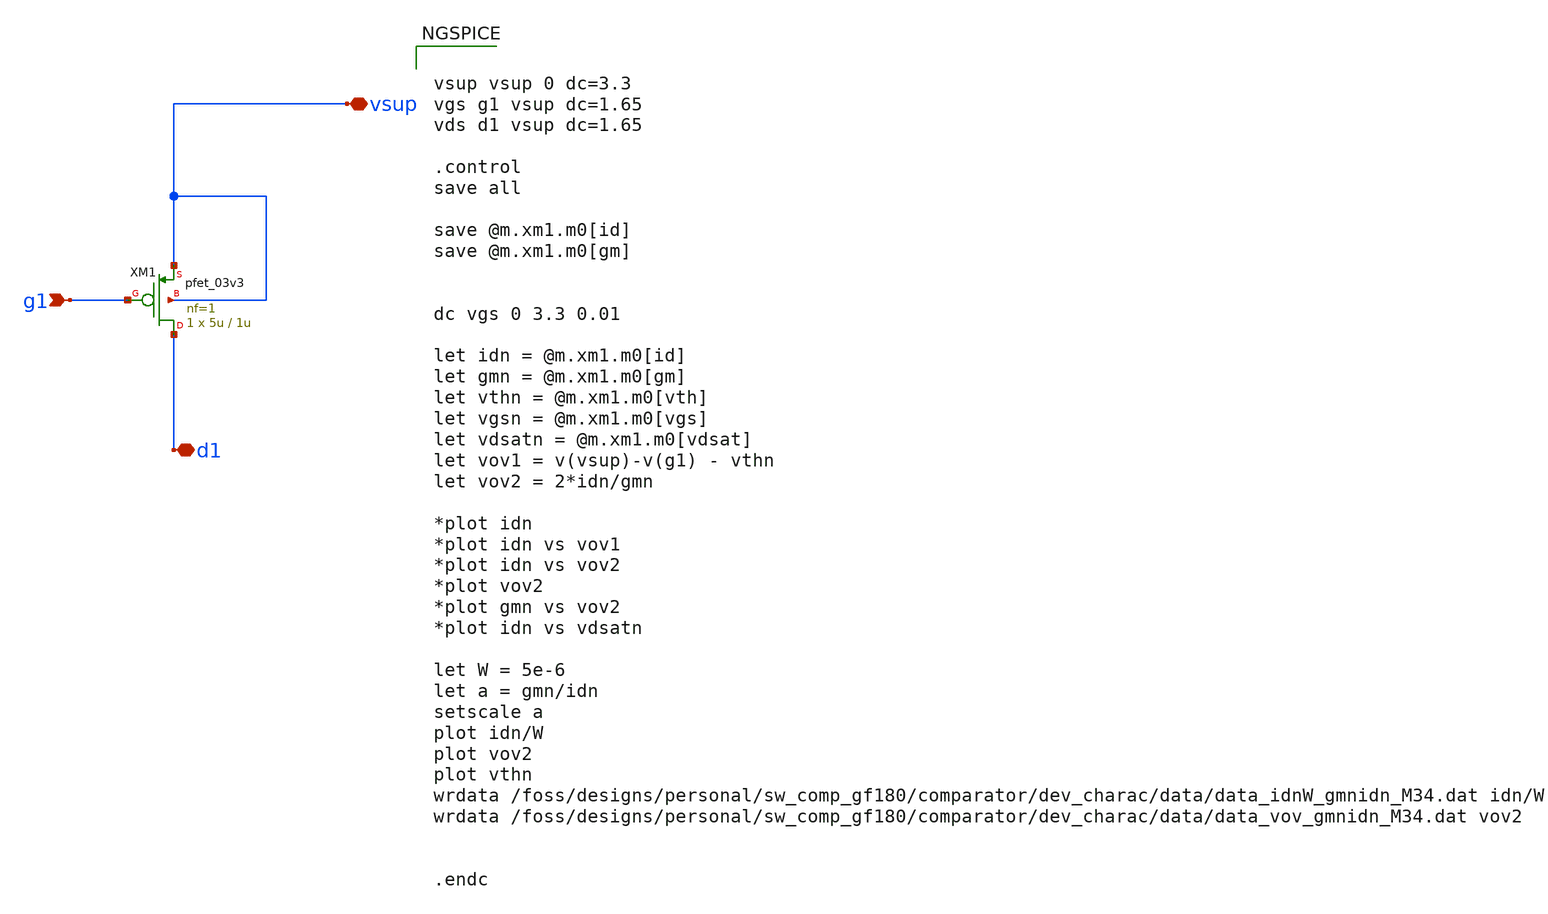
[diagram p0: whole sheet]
** sch_path: xschem/test/dev_charac/pmos_charac_gf180_3p3_M34.sch

.include $env(PDK_ROOT)/$env(PDK)/libs.tech/ngspice/design.ngspice

.lib $env(PDK_ROOT)/$env(PDK)/libs.tech/ngspice/sm141064.ngspice typical
.lib $env(PDK_ROOT)/$env(PDK)/libs.tech/ngspice/sm141064.ngspice mimcap_statistical
.lib $env(PDK_ROOT)/$env(PDK)/libs.tech/ngspice/sm141064.ngspice cap_mim
.lib $env(PDK_ROOT)/$env(PDK)/libs.tech/ngspice/sm141064.ngspice res_typical
.lib $env(PDK_ROOT)/$env(PDK)/libs.tech/ngspice/sm141064.ngspice bjt_typical
.lib $env(PDK_ROOT)/$env(PDK)/libs.tech/ngspice/sm141064.ngspice moscap_typical


**.subckt pmos_charac_gf180_3p3_M34 g1 d1 vsup
*.ipin g1
*.iopin d1
*.iopin vsup
XM1 d1 g1 vsup vsup pfet_03v3 L=1u W=5u nf=1 ad='int((nf+1)/2) * W/nf * 0.18u' as='int((nf+2)/2) * W/nf * 0.18u'
+ pd='2*int((nf+1)/2) * (W/nf + 0.18u)' ps='2*int((nf+2)/2) * (W/nf + 0.18u)' nrd='0.18u / W' nrs='0.18u / W'
+ sa=0 sb=0 sd=0 m=1
**** begin user architecture code


vsup vsup 0 dc=3.3
vgs g1 vsup dc=1.65
vds d1 vsup dc=1.65

.control
save all

save @m.xm1.m0[id]
save @m.xm1.m0[gm]


dc vgs 0 3.3 0.01

let idn = @m.xm1.m0[id]
let gmn = @m.xm1.m0[gm]
let vthn = @m.xm1.m0[vth]
let vgsn = @m.xm1.m0[vgs]
let vdsatn = @m.xm1.m0[vdsat]
let vov1 = v(vsup)-v(g1) - vthn
let vov2 = 2*idn/gmn

*plot idn
*plot idn vs vov1
*plot idn vs vov2
*plot vov2
*plot gmn vs vov2
*plot idn vs vdsatn

let W = 5e-6
let a = gmn/idn
setscale a
plot idn/W
plot vov2
plot vthn
wrdata /foss/designs/personal/sw_comp_gf180/comparator/dev_charac/data/data_idnW_gmnidn_M34.dat
+ idn/W
wrdata /foss/designs/personal/sw_comp_gf180/comparator/dev_charac/data/data_vov_gmnidn_M34.dat vov2


.endc


**** end user architecture code
**.ends
.end
